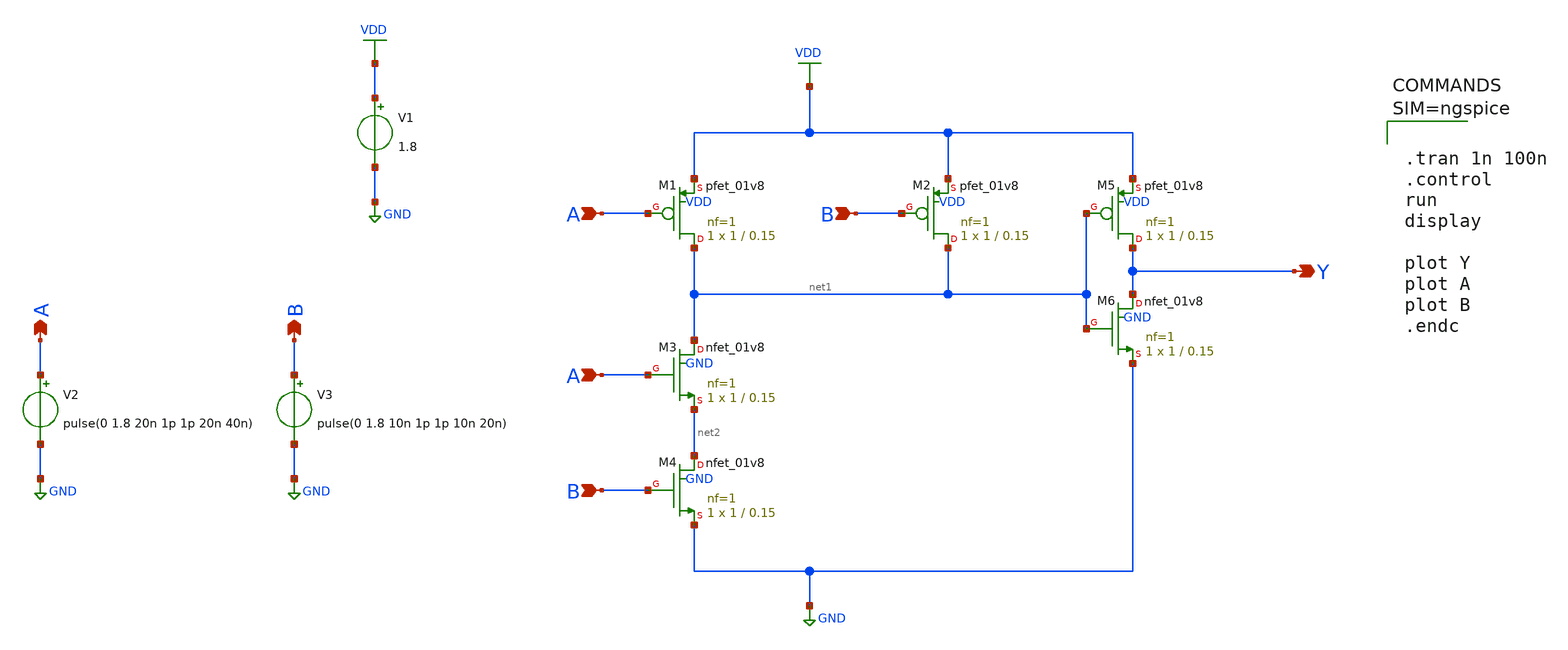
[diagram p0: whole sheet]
** sch_path: Ngspice/AND_Gate/AND_GATE.sch
**.subckt AND_GATE A B A A B B Y
*.opin A
*.opin B
*.ipin A
*.ipin A
*.ipin B
*.ipin B
*.opin Y
V1 VDD GND 1.8
XM1 net1 A VDD VDD sky130_fd_pr__pfet_01v8 L=0.15 W=1 nf=1 ad='int((1 + 1)/2) * 1 / 1 * 0.29' as='int((1 + 2)/2) * 1 / 1 * 0.29'
+ pd='2*int((1 + 1)/2) * (1 / 1 + 0.29)' ps='2*int((1 + 2)/2) * (1 / 1 + 0.29)' nrd='0.29 / 1 ' nrs='0.29 / 1 '
+ sa=0 sb=0 sd=0 mult=1 m=1
XM2 net1 B VDD VDD sky130_fd_pr__pfet_01v8 L=0.15 W=1 nf=1 ad='int((1 + 1)/2) * 1 / 1 * 0.29' as='int((1 + 2)/2) * 1 / 1 * 0.29'
+ pd='2*int((1 + 1)/2) * (1 / 1 + 0.29)' ps='2*int((1 + 2)/2) * (1 / 1 + 0.29)' nrd='0.29 / 1 ' nrs='0.29 / 1 '
+ sa=0 sb=0 sd=0 mult=1 m=1
XM3 net1 A net2 GND sky130_fd_pr__nfet_01v8 L=0.15 W=1 nf=1 ad='int((1 + 1)/2) * 1 / 1 * 0.29' as='int((1 + 2)/2) * 1 / 1 * 0.29'
+ pd='2*int((1 + 1)/2) * (1 / 1 + 0.29)' ps='2*int((1 + 2)/2) * (1 / 1 + 0.29)' nrd='0.29 / 1 ' nrs='0.29 / 1 '
+ sa=0 sb=0 sd=0 mult=1 m=1
XM4 net2 B GND GND sky130_fd_pr__nfet_01v8 L=0.15 W=1 nf=1 ad='int((1 + 1)/2) * 1 / 1 * 0.29' as='int((1 + 2)/2) * 1 / 1 * 0.29'
+ pd='2*int((1 + 1)/2) * (1 / 1 + 0.29)' ps='2*int((1 + 2)/2) * (1 / 1 + 0.29)' nrd='0.29 / 1 ' nrs='0.29 / 1 '
+ sa=0 sb=0 sd=0 mult=1 m=1
XM5 Y net1 VDD VDD sky130_fd_pr__pfet_01v8 L=0.15 W=1 nf=1 ad='int((1 + 1)/2) * 1 / 1 * 0.29' as='int((1 + 2)/2) * 1 / 1 * 0.29'
+ pd='2*int((1 + 1)/2) * (1 / 1 + 0.29)' ps='2*int((1 + 2)/2) * (1 / 1 + 0.29)' nrd='0.29 / 1 ' nrs='0.29 / 1 '
+ sa=0 sb=0 sd=0 mult=1 m=1
XM6 Y net1 GND GND sky130_fd_pr__nfet_01v8 L=0.15 W=1 nf=1 ad='int((1 + 1)/2) * 1 / 1 * 0.29' as='int((1 + 2)/2) * 1 / 1 * 0.29'
+ pd='2*int((1 + 1)/2) * (1 / 1 + 0.29)' ps='2*int((1 + 2)/2) * (1 / 1 + 0.29)' nrd='0.29 / 1 ' nrs='0.29 / 1 '
+ sa=0 sb=0 sd=0 mult=1 m=1
V2 A GND pulse(0 1.8 20n 1p 1p 20n 40n)
V3 B GND pulse(0 1.8 10n 1p 1p 10n 20n)
**** begin user architecture code

** opencircuitdesign pdks install
.lib $::SKYWATER_MODELS/sky130.lib.spice tt




.tran 1n 100n
.control
run
display

plot Y
plot A
plot B
.endc



**** end user architecture code
**.ends
.GLOBAL VDD
.GLOBAL GND
.end
